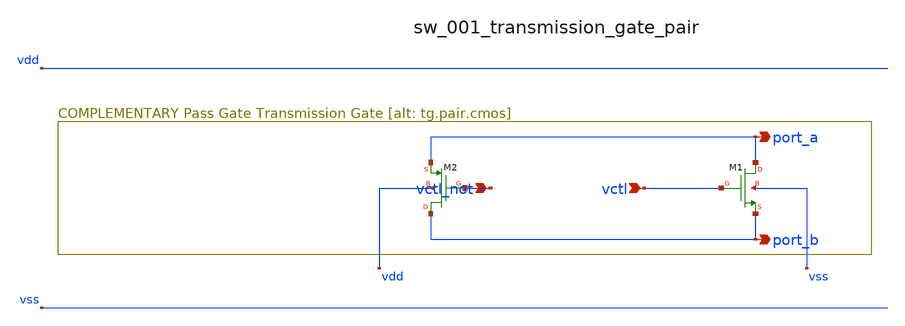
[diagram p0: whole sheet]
** sch_path: analog-db/raw/sw_001_transmission_gate_pair/sw_001_transmission_gate_pair_annotated.sch
**.subckt sw_001_transmission_gate_pair_annotated vctl_not vctl port_a port_b
*.ipin vctl_not
*.ipin vctl
*.opin port_a
*.opin port_b
XM1 port_a vctl port_b vss sg13_lv_nmos w=x_dut_xm1_w l=x_dut_xm1_l ng=1 m=x_dut_xm1_m
XM2 port_b vctl_not port_a vdd sg13_lv_pmos w=x_dut_xm2_w l=x_dut_xm2_l ng=1 m=x_dut_xm2_m
**.ends
.end
